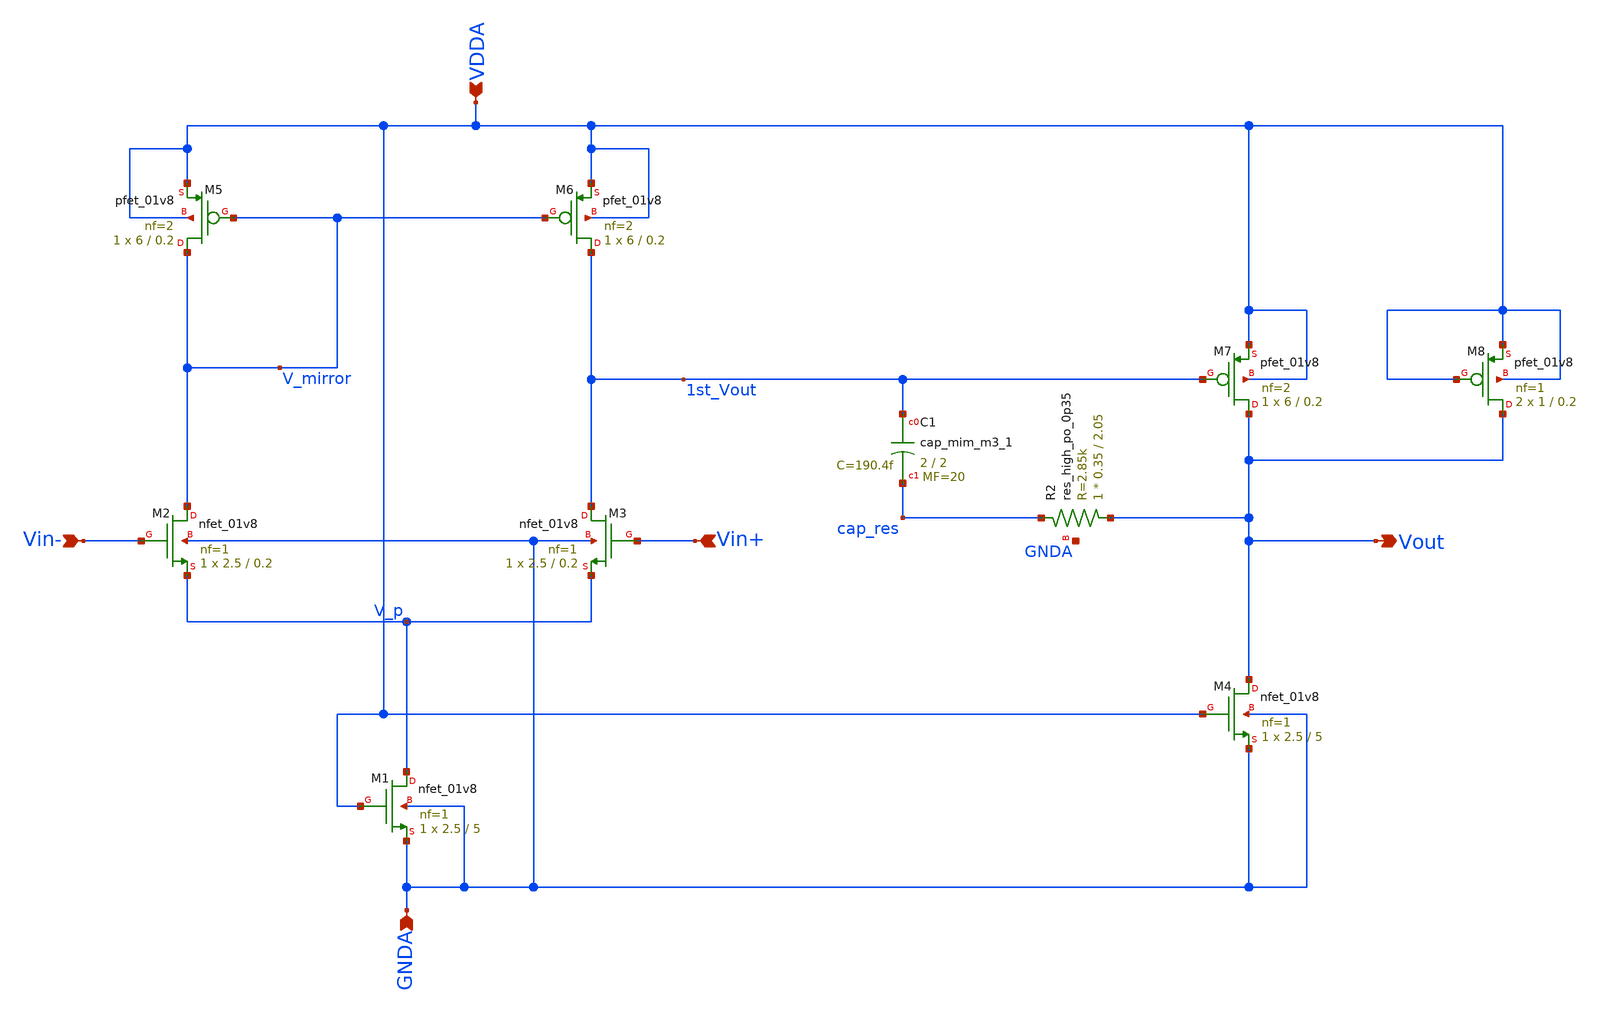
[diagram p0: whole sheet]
** sch_path: projects/bandgapref/xschem_ngspice/new_files/opamp_bandgap_2.sch
**.subckt opamp_bandgap_2 Vin+ Vout Vin- GNDA VDDA
*.ipin Vin+
*.opin Vout
*.ipin Vin-
*.ipin GNDA
*.ipin VDDA
XM1 V_p VDDA GNDA GNDA sky130_fd_pr__nfet_01v8 L=5 W=2.5 nf=1 ad='int((nf+1)/2) * W/nf * 0.29' as='int((nf+2)/2) * W/nf * 0.29'
+ pd='2*int((nf+1)/2) * (W/nf + 0.29)' ps='2*int((nf+2)/2) * (W/nf + 0.29)' nrd='0.29 / W' nrs='0.29 / W'
+ sa=0 sb=0 sd=0 mult=1 m=1
XM2 V_mirror Vin- V_p GNDA sky130_fd_pr__nfet_01v8 L=0.2 W=2.5 nf=1 ad='int((nf+1)/2) * W/nf * 0.29'
+ as='int((nf+2)/2) * W/nf * 0.29' pd='2*int((nf+1)/2) * (W/nf + 0.29)' ps='2*int((nf+2)/2) * (W/nf + 0.29)'
+ nrd='0.29 / W' nrs='0.29 / W' sa=0 sb=0 sd=0 mult=1 m=1
XM3 1st_Vout Vin+ V_p GNDA sky130_fd_pr__nfet_01v8 L=0.2 W=2.5 nf=1 ad='int((nf+1)/2) * W/nf * 0.29'
+ as='int((nf+2)/2) * W/nf * 0.29' pd='2*int((nf+1)/2) * (W/nf + 0.29)' ps='2*int((nf+2)/2) * (W/nf + 0.29)'
+ nrd='0.29 / W' nrs='0.29 / W' sa=0 sb=0 sd=0 mult=1 m=1
XM5 V_mirror V_mirror VDDA VDDA sky130_fd_pr__pfet_01v8 L=0.2 W=6 nf=2 ad='int((nf+1)/2) * W/nf * 0.29'
+ as='int((nf+2)/2) * W/nf * 0.29' pd='2*int((nf+1)/2) * (W/nf + 0.29)' ps='2*int((nf+2)/2) * (W/nf + 0.29)'
+ nrd='0.29 / W' nrs='0.29 / W' sa=0 sb=0 sd=0 mult=1 m=1
XM6 1st_Vout V_mirror VDDA VDDA sky130_fd_pr__pfet_01v8 L=0.2 W=6 nf=2 ad='int((nf+1)/2) * W/nf * 0.29'
+ as='int((nf+2)/2) * W/nf * 0.29' pd='2*int((nf+1)/2) * (W/nf + 0.29)' ps='2*int((nf+2)/2) * (W/nf + 0.29)'
+ nrd='0.29 / W' nrs='0.29 / W' sa=0 sb=0 sd=0 mult=1 m=1
XM4 Vout VDDA GNDA GNDA sky130_fd_pr__nfet_01v8 L=5 W=2.5 nf=1 ad='int((nf+1)/2) * W/nf * 0.29' as='int((nf+2)/2) * W/nf * 0.29'
+ pd='2*int((nf+1)/2) * (W/nf + 0.29)' ps='2*int((nf+2)/2) * (W/nf + 0.29)' nrd='0.29 / W' nrs='0.29 / W'
+ sa=0 sb=0 sd=0 mult=1 m=1
XM7 Vout 1st_Vout VDDA VDDA sky130_fd_pr__pfet_01v8 L=0.2 W=6 nf=2 ad='int((nf+1)/2) * W/nf * 0.29' as='int((nf+2)/2) * W/nf * 0.29'
+ pd='2*int((nf+1)/2) * (W/nf + 0.29)' ps='2*int((nf+2)/2) * (W/nf + 0.29)' nrd='0.29 / W' nrs='0.29 / W'
+ sa=0 sb=0 sd=0 mult=1 m=1
XC1 1st_Vout cap_res sky130_fd_pr__cap_mim_m3_1 W=2 L=2 MF=20 m=20
XM8 Vout VDDA VDDA VDDA sky130_fd_pr__pfet_01v8 L=0.2 W=1 nf=1 ad='int((nf+1)/2) * W/nf * 0.29' as='int((nf+2)/2) * W/nf * 0.29'
+ pd='2*int((nf+1)/2) * (W/nf + 0.29)' ps='2*int((nf+2)/2) * (W/nf + 0.29)' nrd='0.29 / W' nrs='0.29 / W'
+ sa=0 sb=0 sd=0 mult=2 m=2
XR2 Vout cap_res GNDA sky130_fd_pr__res_high_po_0p35 L=2.05 mult=1 m=1
**.ends
.end
